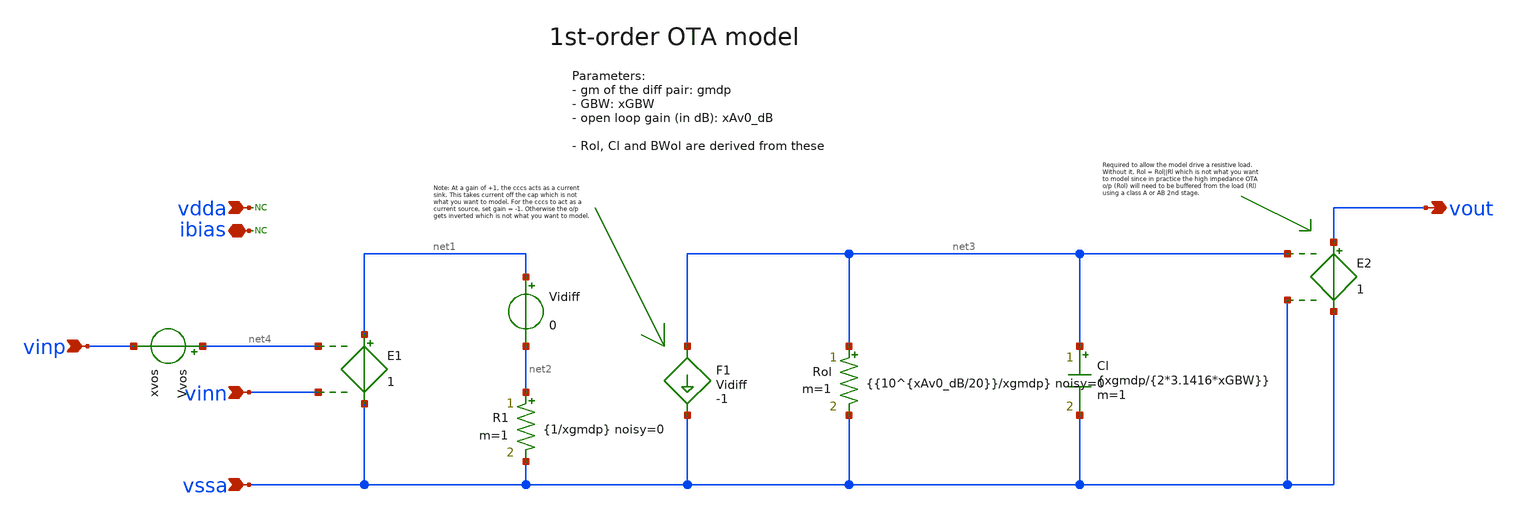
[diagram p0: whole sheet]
** sch_path: Design_Review_1/Testbench_3_tb_sunrise_ina_CMR_idealR/OTA_ideal_order1_element_wos.sch
**.subckt OTA_ideal_order1_element_wos ibias vdda vssa vinp vinn vout
*.iopin ibias
*.ipin vdda
*.ipin vssa
*.ipin vinp
*.ipin vinn
*.opin vout
* noconn vdda
* noconn ibias
F1 net3 vssa Vidiff -1
E1 net1 vssa net4 vinn 1
Vidiff net1 net2 0
R1 net2 vssa {1/xgmdp} noisy=0 m=1
Cl net3 vssa {xgmdp/{2*3.1416*xGBW}} m=1
Rol net3 vssa {{10^{xAv0_dB/20}}/xgmdp} noisy=0 m=1
E2 vout vssa net3 vssa 1
Vvos net4 vinp xvos
**.ends
.end
